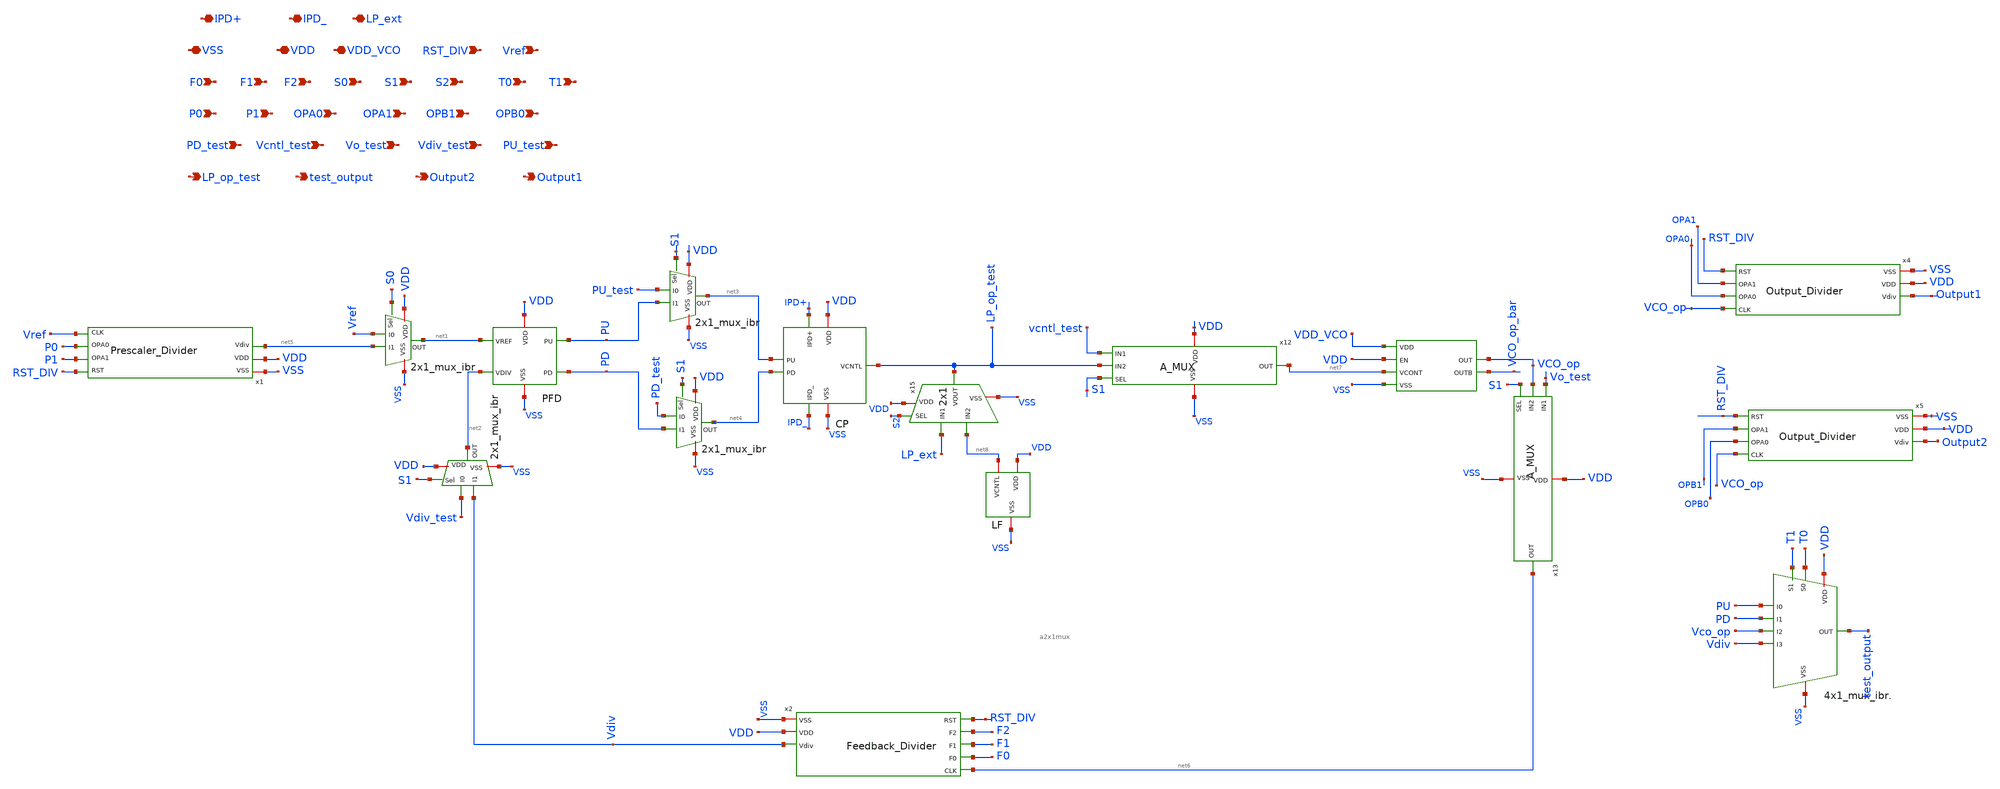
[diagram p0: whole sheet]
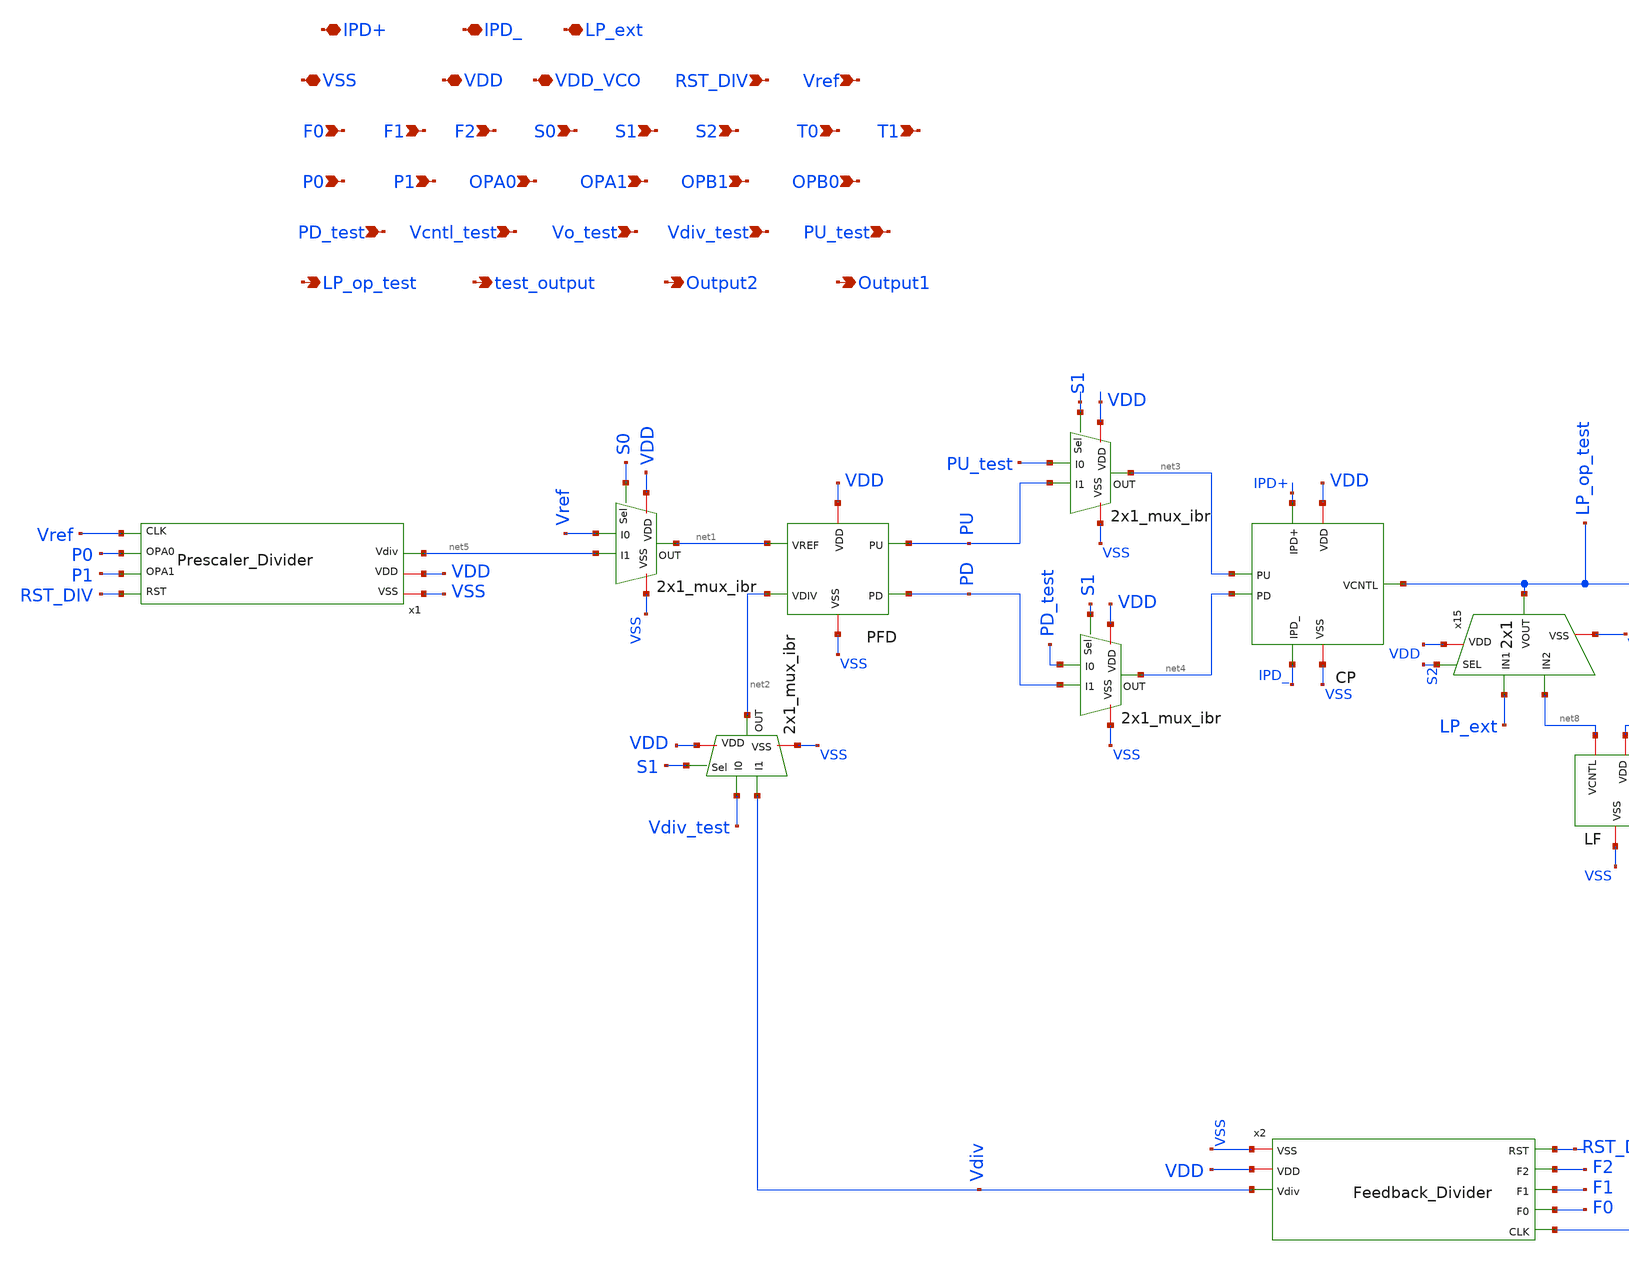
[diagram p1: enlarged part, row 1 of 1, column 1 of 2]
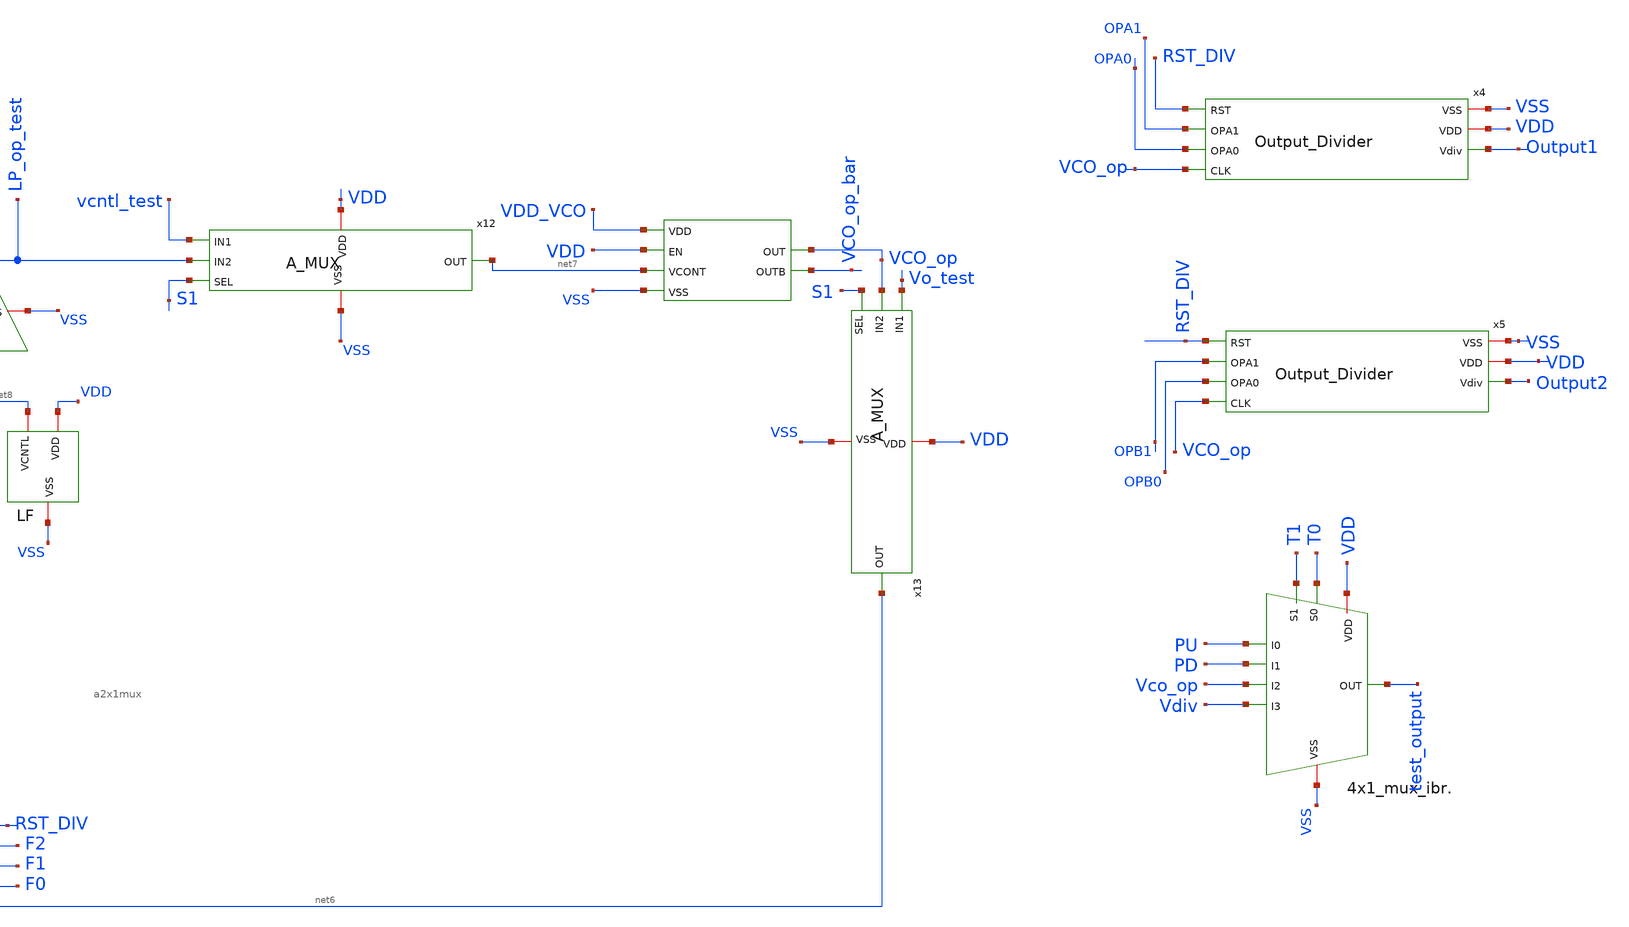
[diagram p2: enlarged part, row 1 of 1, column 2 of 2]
** sch_path: Clock_Generator_PAKISTAN_02/Schematics/PLL_12.sch
**.subckt PLL_12 S1 S0 T0 T1 VDD VDD_VCO Vref F1 F2 P0 P1 OPA0 RST_DIV F0 OPA1 OPB1 OPB0 Vdiv_test
*+ PU_test PD_test Vcntl_test Vo_test LP_op_test test_output Output2 Output1 VSS S2 IPD+ IPD_ LP_ext
*.ipin S1
*.ipin S0
*.ipin T0
*.ipin T1
*.iopin VDD
*.iopin VDD_VCO
*.ipin Vref
*.ipin F1
*.ipin F2
*.ipin P0
*.ipin P1
*.ipin OPA0
*.ipin RST_DIV
*.ipin F0
*.ipin OPA1
*.ipin OPB1
*.ipin OPB0
*.ipin Vdiv_test
*.ipin PU_test
*.ipin PD_test
*.ipin Vcntl_test
*.ipin Vo_test
*.opin LP_op_test
*.opin test_output
*.opin Output2
*.opin Output1
*.iopin VSS
*.ipin S2
*.iopin IPD+
*.iopin IPD_
*.iopin LP_ext
x3 VSS net1 net2 PU PD VDD PFD
x2 VSS VDD RST_DIV Vdiv F2 F1 F0 net6 Feedback_Divider
x5 VSS VDD RST_DIV Output2 OPB1 OPB0 VCO_op Output_Divider
x6 IPD+ IPD_ net3 net4 LP_op_test VSS VDD CP
x4 VSS VDD RST_DIV Output1 OPA1 OPA0 VCO_op Output_Divider
x12 VDD VSS vcntl_test LP_op_test S1 net7 A_MUX
x13 VDD VSS Vo_test VCO_op S1 net6 A_MUX
x7 net8 VDD VSS LF
x15 LP_ext VDD LP_op_test net9 VSS net8 a2x1mux
x16 VDD T1 VSS Vco_op Vdiv T0 PU PD test_output 4x1_mux_ibr.
x1 VSS VDD RST_DIV net5 P1 P0 Vref Prescaler_Divider
x11 VSS S0 net1 Vref net5 VDD 2x1_mux_ibr
x14 VSS S1 net2 Vdiv_test Vdiv VDD 2x1_mux_ibr
x9 VSS S1 net3 PU_test PU VDD 2x1_mux_ibr
x10 VSS S1 net4 PD_test PD VDD 2x1_mux_ibr
x8 VDD_VCO VDD VCO_op VCO_op_bar net7 VSS VCO
**.ends
.end
